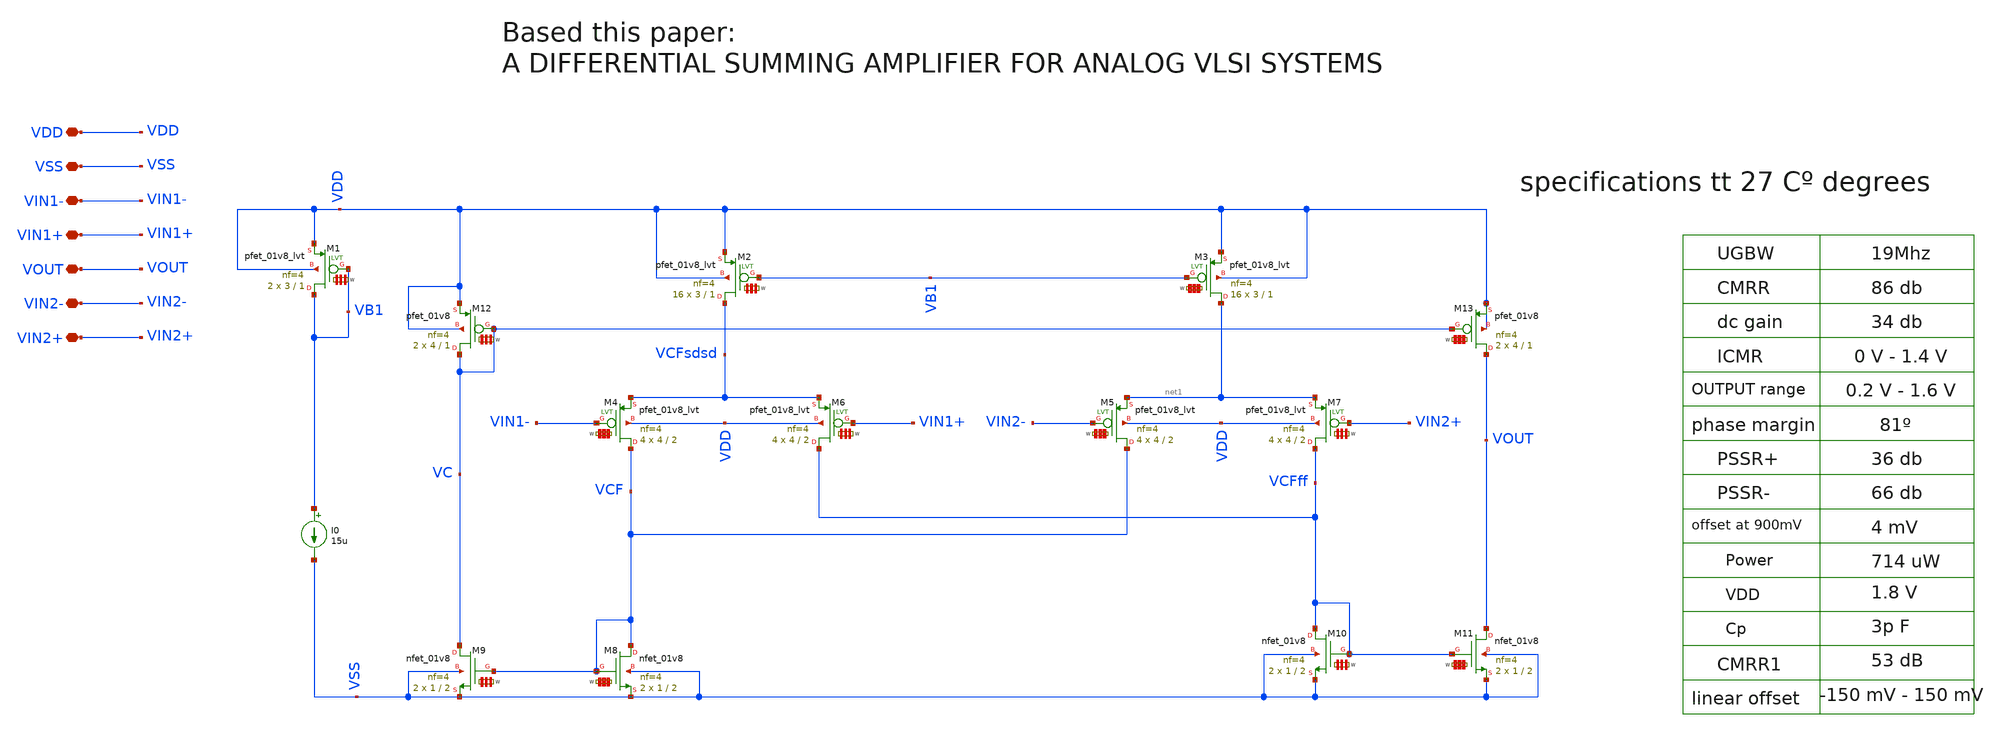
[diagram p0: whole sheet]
** sch_path: my_ip/LIB/DDA001_PMOS_1.8_sky130A .sch
**.subckt DDA001_PMOS_1.8_sky130A  VDD VSS VIN1- VIN1+ VOUT VIN2- VIN2+
*.iopin VDD
*.iopin VSS
*.iopin VIN1-
*.iopin VIN1+
*.iopin VOUT
*.iopin VIN2-
*.iopin VIN2+
I0 VB1 VSS 15u
XM1 VB1 VB1 VDD VDD sky130_fd_pr__pfet_01v8_lvt L=1 W='3 * 4 ' nf=4 ad='int((4 + 1)/2) * 3 / 4 * 0.29'
+ as='int((4 + 2)/2) * 3 / 4 * 0.29' pd='2*int((4 + 1)/2) * (3 / 4 + 0.29)' ps='2*int((4 + 2)/2) * (3 / 4 + 0.29)'
+ nrd='0.29 / 3 ' nrs='0.29 / 3 ' sa=0 sb=0 sd=0 mult=2 m=2
XM2 VCFsdsd VB1 VDD VDD sky130_fd_pr__pfet_01v8_lvt L=1 W='3 * 4 ' nf=4 ad='int((4 + 1)/2) * 3 / 4 * 0.29'
+ as='int((4 + 2)/2) * 3 / 4 * 0.29' pd='2*int((4 + 1)/2) * (3 / 4 + 0.29)' ps='2*int((4 + 2)/2) * (3 / 4 + 0.29)'
+ nrd='0.29 / 3 ' nrs='0.29 / 3 ' sa=0 sb=0 sd=0 mult=16 m=16
XM3 net1 VB1 VDD VDD sky130_fd_pr__pfet_01v8_lvt L=1 W='3 * 4 ' nf=4 ad='int((4 + 1)/2) * 3 / 4 * 0.29'
+ as='int((4 + 2)/2) * 3 / 4 * 0.29' pd='2*int((4 + 1)/2) * (3 / 4 + 0.29)' ps='2*int((4 + 2)/2) * (3 / 4 + 0.29)'
+ nrd='0.29 / 3 ' nrs='0.29 / 3 ' sa=0 sb=0 sd=0 mult=16 m=16
XM4 VCF VIN1- VCFsdsd VDD sky130_fd_pr__pfet_01v8_lvt L=2 W='4 * 4 ' nf=4 ad='int((4 + 1)/2) * 4 / 4 * 0.29'
+ as='int((4 + 2)/2) * 4 / 4 * 0.29' pd='2*int((4 + 1)/2) * (4 / 4 + 0.29)' ps='2*int((4 + 2)/2) * (4 / 4 + 0.29)'
+ nrd='0.29 / 4 ' nrs='0.29 / 4 ' sa=0 sb=0 sd=0 mult=4 m=4
XM8 VCF VCF VSS VSS sky130_fd_pr__nfet_01v8 L=2 W='1 * 4 ' nf=4 ad='int((4 + 1)/2) * 1 / 4 * 0.29' as='int((4 + 2)/2) * 1 / 4 * 0.29'
+ pd='2*int((4 + 1)/2) * (1 / 4 + 0.29)' ps='2*int((4 + 2)/2) * (1 / 4 + 0.29)' nrd='0.29 / 1 ' nrs='0.29 / 1 '
+ sa=0 sb=0 sd=0 mult=2 m=2
XM9 VC VCF VSS VSS sky130_fd_pr__nfet_01v8 L=2 W='1 * 4 ' nf=4 ad='int((4 + 1)/2) * 1 / 4 * 0.29' as='int((4 + 2)/2) * 1 / 4 * 0.29'
+ pd='2*int((4 + 1)/2) * (1 / 4 + 0.29)' ps='2*int((4 + 2)/2) * (1 / 4 + 0.29)' nrd='0.29 / 1 ' nrs='0.29 / 1 '
+ sa=0 sb=0 sd=0 mult=2 m=2
XM10 VCFff VCFff VSS VSS sky130_fd_pr__nfet_01v8 L=2 W='1 * 4 ' nf=4 ad='int((4 + 1)/2) * 1 / 4 * 0.29'
+ as='int((4 + 2)/2) * 1 / 4 * 0.29' pd='2*int((4 + 1)/2) * (1 / 4 + 0.29)' ps='2*int((4 + 2)/2) * (1 / 4 + 0.29)'
+ nrd='0.29 / 1 ' nrs='0.29 / 1 ' sa=0 sb=0 sd=0 mult=2 m=2
XM11 VOUT VCFff VSS VSS sky130_fd_pr__nfet_01v8 L=2 W='1 * 4 ' nf=4 ad='int((4 + 1)/2) * 1 / 4 * 0.29'
+ as='int((4 + 2)/2) * 1 / 4 * 0.29' pd='2*int((4 + 1)/2) * (1 / 4 + 0.29)' ps='2*int((4 + 2)/2) * (1 / 4 + 0.29)'
+ nrd='0.29 / 1 ' nrs='0.29 / 1 ' sa=0 sb=0 sd=0 mult=2 m=2
XM12 VC VC VDD VDD sky130_fd_pr__pfet_01v8 L=1 W='4 * 4 ' nf=4 ad= as='int((4 + 2)/2) * 4 * 0.29' pd='2*int((4 + 1)/2) * (4 + 0.29)'
+ ps='2*int((4 + 2)/2) * (4 + 0.29)' nrd='0.29 / 4 / 4 ' nrs='0.29 / 4 / 4 ' sa=0 sb=0 sd=0 mult=2 m=2
XM13 VOUT VC VDD VDD sky130_fd_pr__pfet_01v8 L=1 W='4 * 4 ' nf=4 ad= as='int((4 + 2)/2) * 4 * 0.29' pd='2*int((4 + 1)/2) * (4 + 0.29)'
+ ps='2*int((4 + 2)/2) * (4 + 0.29)' nrd='0.29 / 4 / 4 ' nrs='0.29 / 4 / 4 ' sa=0 sb=0 sd=0 mult=2 m=2
XM5 VCF VIN2- net1 VDD sky130_fd_pr__pfet_01v8_lvt L=2 W='4 * 4 ' nf=4 ad='int((4 + 1)/2) * 4 / 4 * 0.29'
+ as='int((4 + 2)/2) * 4 / 4 * 0.29' pd='2*int((4 + 1)/2) * (4 / 4 + 0.29)' ps='2*int((4 + 2)/2) * (4 / 4 + 0.29)'
+ nrd='0.29 / 4 ' nrs='0.29 / 4 ' sa=0 sb=0 sd=0 mult=4 m=4
XM6 VCFff VIN1+ VCFsdsd VDD sky130_fd_pr__pfet_01v8_lvt L=2 W='4 * 4 ' nf=4 ad='int((4 + 1)/2) * 4 / 4 * 0.29'
+ as='int((4 + 2)/2) * 4 / 4 * 0.29' pd='2*int((4 + 1)/2) * (4 / 4 + 0.29)' ps='2*int((4 + 2)/2) * (4 / 4 + 0.29)'
+ nrd='0.29 / 4 ' nrs='0.29 / 4 ' sa=0 sb=0 sd=0 mult=4 m=4
XM7 VCFff VIN2+ net1 VDD sky130_fd_pr__pfet_01v8_lvt L=2 W='4 * 4 ' nf=4 ad='int((4 + 1)/2) * 4 / 4 * 0.29'
+ as='int((4 + 2)/2) * 4 / 4 * 0.29' pd='2*int((4 + 1)/2) * (4 / 4 + 0.29)' ps='2*int((4 + 2)/2) * (4 / 4 + 0.29)'
+ nrd='0.29 / 4 ' nrs='0.29 / 4 ' sa=0 sb=0 sd=0 mult=4 m=4
**.ends
.end
